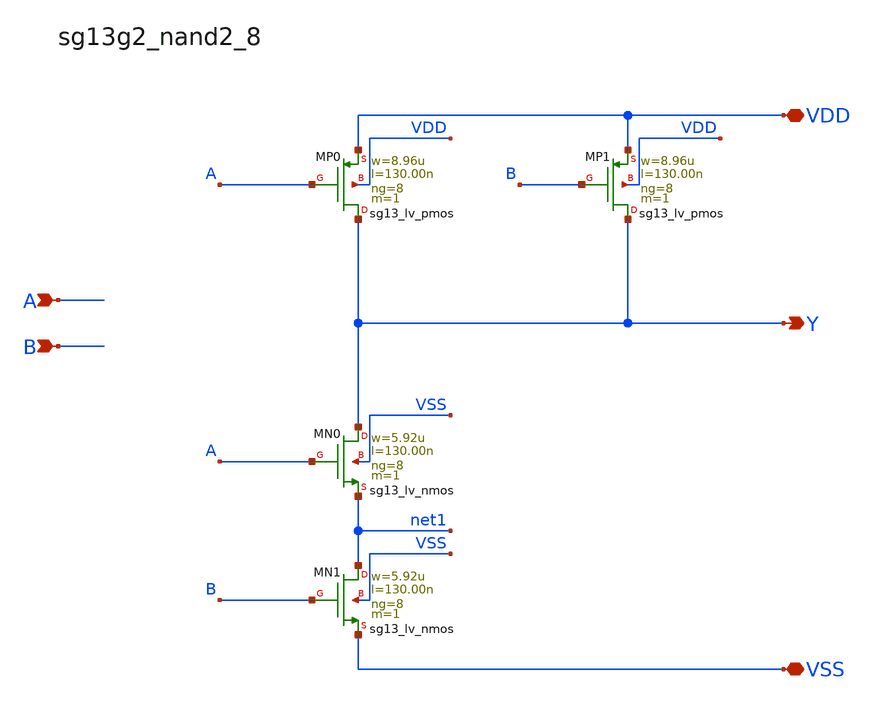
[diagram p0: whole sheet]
** sch_path: outputs/sg13g2_cells/cells/sg13g2_nand2_8/sg13g2_nand2_8.sch
**.subckt sg13g2_nand2_8 Y A B VDD VSS
*.opin Y
*.ipin A
*.ipin B
*.iopin VDD
*.iopin VSS
XMP1 Y B VDD VDD sg13_lv_pmos w=8.96u l=130.00n ng=8 m=1 mm_ok=1
XMP0 Y A VDD VDD sg13_lv_pmos w=8.96u l=130.00n ng=8 m=1 mm_ok=1
XMN1 net1 B VSS VSS sg13_lv_nmos w=5.92u l=130.00n ng=8 m=1 mm_ok=1
XMN0 Y A net1 VSS sg13_lv_nmos w=5.92u l=130.00n ng=8 m=1 mm_ok=1
**.ends
.end
